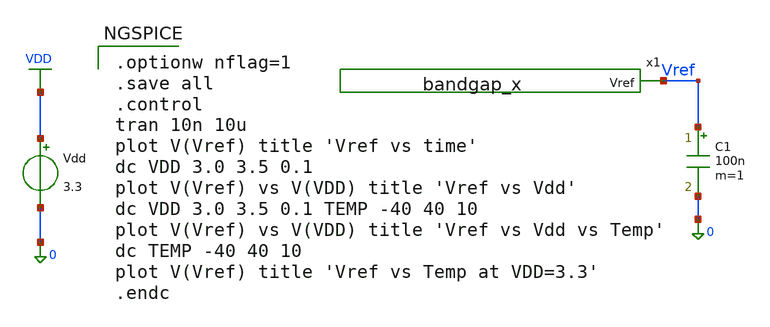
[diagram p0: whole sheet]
** sch_path: xschem/bandgap_x_tb.sch
**.subckt bandgap_x_tb
x1 Vref bandgap_x
Vdd VDD 0 3.3
C1 Vref 0 100n m=1
**** begin user architecture code

.optionw nflag=1
.save all
.control
tran 10n 10u
plot V(Vref) title 'Vref vs time'
dc VDD 3.0 3.5 0.1
plot V(Vref) vs V(VDD) title 'Vref vs Vdd'
dc VDD 3.0 3.5 0.1 TEMP -40 40 10
plot V(Vref) vs V(VDD) title 'Vref vs Vdd vs Temp'
dc TEMP -40 40 10
plot V(Vref) title 'Vref vs Temp at VDD=3.3'
.endc


** opencircuitdesign pdks install
.lib $::SKYWATER_MODELS/sky130.lib.spice tt

**** end user architecture code
**.ends

* expanding   symbol:  bandgap_x.sym # of pins=1
** sym_path: xschem/bandgap_x.sym
** sch_path: xschem/bandgap_x.sch
.subckt bandgap_x Vref
*.opin Vref
XM2 net3 net14 net1 VDD sky130_fd_pr__pfet_g5v0d10v5 L=1 W=20 nf=1 ad='int((1 + 1)/2) * 20 / 1 * 0.29'
+ as='int((1 + 2)/2) * 20 / 1 * 0.29' pd='2*int((1 + 1)/2) * (20 / 1 + 0.29)' ps='2*int((1 + 2)/2) * (20 / 1 + 0.29)'
+ nrd='0.29 / 20 ' nrs='0.29 / 20 ' sa=0 sb=0 sd=0 mult=1 m=1
XM1 net2 net12 net1 VDD sky130_fd_pr__pfet_g5v0d10v5 L=1 W=20 nf=1 ad='int((1 + 1)/2) * 20 / 1 * 0.29'
+ as='int((1 + 2)/2) * 20 / 1 * 0.29' pd='2*int((1 + 1)/2) * (20 / 1 + 0.29)' ps='2*int((1 + 2)/2) * (20 / 1 + 0.29)'
+ nrd='0.29 / 20 ' nrs='0.29 / 20 ' sa=0 sb=0 sd=0 mult=1 m=1
XM3 net2 net3 0 0 sky130_fd_pr__nfet_g5v0d10v5 L=1 W=20 nf=1 ad='int((1 + 1)/2) * 20 / 1 * 0.29' as='int((1 + 2)/2) * 20 / 1 * 0.29'
+ pd='2*int((1 + 1)/2) * (20 / 1 + 0.29)' ps='2*int((1 + 2)/2) * (20 / 1 + 0.29)' nrd='0.29 / 20 ' nrs='0.29 / 20 '
+ sa=0 sb=0 sd=0 mult=1 m=1
XM4 net3 net3 0 0 sky130_fd_pr__nfet_g5v0d10v5 L=1 W=20 nf=1 ad='int((1 + 1)/2) * 20 / 1 * 0.29' as='int((1 + 2)/2) * 20 / 1 * 0.29'
+ pd='2*int((1 + 1)/2) * (20 / 1 + 0.29)' ps='2*int((1 + 2)/2) * (20 / 1 + 0.29)' nrd='0.29 / 20 ' nrs='0.29 / 20 '
+ sa=0 sb=0 sd=0 mult=1 m=1
XM5 net6 net6 VDD VDD sky130_fd_pr__pfet_g5v0d10v5 L=1 W=1 nf=1 ad='int((1 + 1)/2) * 1 / 1 * 0.29' as='int((1 + 2)/2) * 1 / 1 * 0.29'
+ pd='2*int((1 + 1)/2) * (1 / 1 + 0.29)' ps='2*int((1 + 2)/2) * (1 / 1 + 0.29)' nrd='0.29 / 1 ' nrs='0.29 / 1 '
+ sa=0 sb=0 sd=0 mult=1 m=1
XM6 net6 Vref net7 0 sky130_fd_pr__nfet_g5v0d10v5 L=1 W=5 nf=1 ad='int((1 + 1)/2) * 5 / 1 * 0.29' as='int((1 + 2)/2) * 5 / 1 * 0.29'
+ pd='2*int((1 + 1)/2) * (5 / 1 + 0.29)' ps='2*int((1 + 2)/2) * (5 / 1 + 0.29)' nrd='0.29 / 5 ' nrs='0.29 / 5 '
+ sa=0 sb=0 sd=0 mult=1 m=1
XM7a net5 net5 net8 0 sky130_fd_pr__nfet_g5v0d10v5 L=20 W=0.5 nf=1 ad='int((1 + 1)/2) * 0.5 / 1 * 0.29'
+ as='int((1 + 2)/2) * 0.5 / 1 * 0.29' pd='2*int((1 + 1)/2) * (0.5 / 1 + 0.29)' ps='2*int((1 + 2)/2) * (0.5 / 1 + 0.29)'
+ nrd='0.29 / 0.5 ' nrs='0.29 / 0.5 ' sa=0 sb=0 sd=0 mult=1 m=1
XM8 net5 net6 VDD VDD sky130_fd_pr__pfet_g5v0d10v5 L=1 W=1 nf=1 ad='int((1 + 1)/2) * 1 / 1 * 0.29' as='int((1 + 2)/2) * 1 / 1 * 0.29'
+ pd='2*int((1 + 1)/2) * (1 / 1 + 0.29)' ps='2*int((1 + 2)/2) * (1 / 1 + 0.29)' nrd='0.29 / 1 ' nrs='0.29 / 1 '
+ sa=0 sb=0 sd=0 mult=1 m=1
XM9 net5 Vref net4 0 sky130_fd_pr__nfet_g5v0d10v5 L=1 W=20 nf=1 ad='int((1 + 1)/2) * 20 / 1 * 0.29' as='int((1 + 2)/2) * 20 / 1 * 0.29'
+ pd='2*int((1 + 1)/2) * (20 / 1 + 0.29)' ps='2*int((1 + 2)/2) * (20 / 1 + 0.29)' nrd='0.29 / 20 ' nrs='0.29 / 20 '
+ sa=0 sb=0 sd=0 mult=1 m=1
XM10 net4 net2 0 0 sky130_fd_pr__nfet_g5v0d10v5 L=1 W=20 nf=1 ad='int((1 + 1)/2) * 20 / 1 * 0.29' as='int((1 + 2)/2) * 20 / 1 * 0.29'
+ pd='2*int((1 + 1)/2) * (20 / 1 + 0.29)' ps='2*int((1 + 2)/2) * (20 / 1 + 0.29)' nrd='0.29 / 20 ' nrs='0.29 / 20 '
+ sa=0 sb=0 sd=0 mult=1 m=1
XM11 net1 net6 VDD VDD sky130_fd_pr__pfet_g5v0d10v5 L=1 W=1 nf=1 ad='int((1 + 1)/2) * 1 / 1 * 0.29' as='int((1 + 2)/2) * 1 / 1 * 0.29'
+ pd='2*int((1 + 1)/2) * (1 / 1 + 0.29)' ps='2*int((1 + 2)/2) * (1 / 1 + 0.29)' nrd='0.29 / 1 ' nrs='0.29 / 1 '
+ sa=0 sb=0 sd=0 mult=1 m=1
XM12 Vref net5 VDD VDD sky130_fd_pr__pfet_g5v0d10v5 L=0.5 W=20 nf=1 ad='int((1 + 1)/2) * 20 / 1 * 0.29'
+ as='int((1 + 2)/2) * 20 / 1 * 0.29' pd='2*int((1 + 1)/2) * (20 / 1 + 0.29)' ps='2*int((1 + 2)/2) * (20 / 1 + 0.29)'
+ nrd='0.29 / 20 ' nrs='0.29 / 20 ' sa=0 sb=0 sd=0 mult=1 m=1
XR1 net14 Vref 0 sky130_fd_pr__res_high_po_0p35 L=22 mult=1 m=1
XR2 net12 Vref 0 sky130_fd_pr__res_high_po_0p35 L=22 mult=1 m=1
XR3 net13 net12 0 sky130_fd_pr__res_high_po_0p35 L=3 mult=1 m=1
XR4 0 net7 0 sky130_fd_pr__res_high_po_0p35 L=44 mult=1 m=1
XQ1 0 0 net13 sky130_fd_pr__pnp_05v5_W3p40L3p40 m=24
XQ2 0 0 net14 sky130_fd_pr__pnp_05v5_W3p40L3p40 m=1
XM7b net8 net5 net9 0 sky130_fd_pr__nfet_g5v0d10v5 L=20 W=0.5 nf=1 ad='int((1 + 1)/2) * 0.5 / 1 * 0.29'
+ as='int((1 + 2)/2) * 0.5 / 1 * 0.29' pd='2*int((1 + 1)/2) * (0.5 / 1 + 0.29)' ps='2*int((1 + 2)/2) * (0.5 / 1 + 0.29)'
+ nrd='0.29 / 0.5 ' nrs='0.29 / 0.5 ' sa=0 sb=0 sd=0 mult=1 m=1
XM7c net9 net5 net10 0 sky130_fd_pr__nfet_g5v0d10v5 L=20 W=0.5 nf=1 ad='int((1 + 1)/2) * 0.5 / 1 * 0.29'
+ as='int((1 + 2)/2) * 0.5 / 1 * 0.29' pd='2*int((1 + 1)/2) * (0.5 / 1 + 0.29)' ps='2*int((1 + 2)/2) * (0.5 / 1 + 0.29)'
+ nrd='0.29 / 0.5 ' nrs='0.29 / 0.5 ' sa=0 sb=0 sd=0 mult=1 m=1
XM7d net10 net5 net11 0 sky130_fd_pr__nfet_g5v0d10v5 L=20 W=0.5 nf=1 ad='int((1 + 1)/2) * 0.5 / 1 * 0.29'
+ as='int((1 + 2)/2) * 0.5 / 1 * 0.29' pd='2*int((1 + 1)/2) * (0.5 / 1 + 0.29)' ps='2*int((1 + 2)/2) * (0.5 / 1 + 0.29)'
+ nrd='0.29 / 0.5 ' nrs='0.29 / 0.5 ' sa=0 sb=0 sd=0 mult=1 m=1
XM7e net11 net5 0 0 sky130_fd_pr__nfet_g5v0d10v5 L=20 W=0.5 nf=1 ad='int((1 + 1)/2) * 0.5 / 1 * 0.29'
+ as='int((1 + 2)/2) * 0.5 / 1 * 0.29' pd='2*int((1 + 1)/2) * (0.5 / 1 + 0.29)' ps='2*int((1 + 2)/2) * (0.5 / 1 + 0.29)'
+ nrd='0.29 / 0.5 ' nrs='0.29 / 0.5 ' sa=0 sb=0 sd=0 mult=1 m=1
.ends

.GLOBAL VDD
.end
